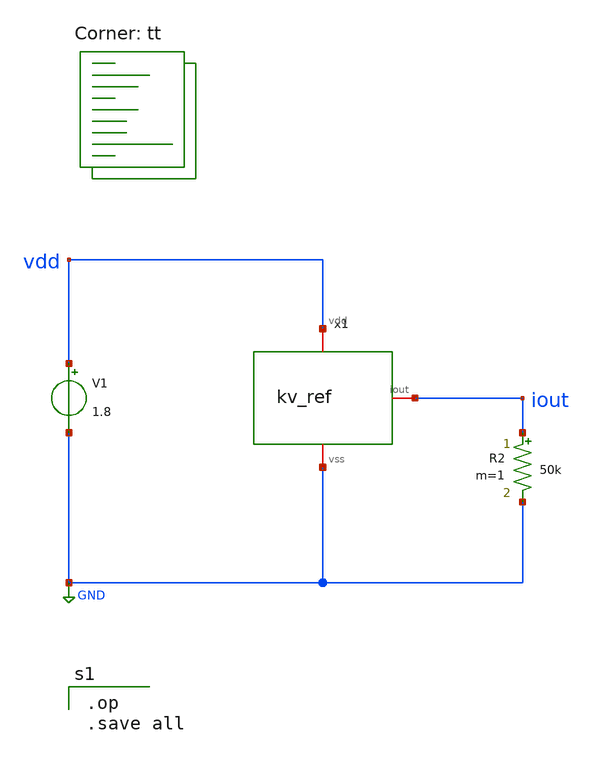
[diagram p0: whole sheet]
** sch_path: examples/demo_tapeout/xschem/tb_ref.sch
**.subckt tb_ref
V1 vdd GND 1.8
x1 vdd GND iout kv_ref
R2 iout GND 50k m=1
**** begin user architecture code
.lib $::SKYWATER_MODELS/sky130.lib.spice tt

.op
.save all

**** end user architecture code
**.ends

* expanding   symbol:  kv_ref.sym # of pins=3
** sym_path: examples/demo_tapeout/xschem/kv_ref.sym
** sch_path: examples/demo_tapeout/xschem/kv_ref.sch
.subckt kv_ref vdd vss iout
*.iopin vdd
*.iopin vss
*.iopin iout
XM3 n1 n2 vdd vdd sky130_fd_pr__pfet_01v8 L=2 W=8 nf=1 ad='int((nf+1)/2) * W/nf * 0.29' as='int((nf+2)/2) * W/nf * 0.29'
+ pd='2*int((nf+1)/2) * (W/nf + 0.29)' ps='2*int((nf+2)/2) * (W/nf + 0.29)' nrd='0.29 / W' nrs='0.29 / W'
+ sa=0 sb=0 sd=0 mult=1 m=1
XM4 n2 n2 vdd vdd sky130_fd_pr__pfet_01v8 L=2 W=8 nf=1 ad='int((nf+1)/2) * W/nf * 0.29' as='int((nf+2)/2) * W/nf * 0.29'
+ pd='2*int((nf+1)/2) * (W/nf + 0.29)' ps='2*int((nf+2)/2) * (W/nf + 0.29)' nrd='0.29 / W' nrs='0.29 / W'
+ sa=0 sb=0 sd=0 mult=1 m=1
XM5 iout n2 vdd vdd sky130_fd_pr__pfet_01v8 L=2 W=8 nf=1 ad='int((nf+1)/2) * W/nf * 0.29' as='int((nf+2)/2) * W/nf * 0.29'
+ pd='2*int((nf+1)/2) * (W/nf + 0.29)' ps='2*int((nf+2)/2) * (W/nf + 0.29)' nrd='0.29 / W' nrs='0.29 / W'
+ sa=0 sb=0 sd=0 mult=1 m=1
XM1 n1 n1 vss vss sky130_fd_pr__nfet_01v8 L=2 W=4 nf=1 ad='int((1 + 1)/2) * 4 / 1 * 0.29' as='int((1 + 2)/2) * 4 / 1 * 0.29'
+ pd='2*int((1 + 1)/2) * (4 / 1 + 0.29)' ps='2*int((1 + 2)/2) * (4 / 1 + 0.29)' nrd='0.29 / 4 ' nrs='0.29 / 4 '
+ sa=0 sb=0 sd=0 mult=1 m=1
XM2 n2 n1 s2 vss sky130_fd_pr__nfet_01v8 L=2 W=16 nf=1 ad='int((1 + 1)/2) * 16 / 1 * 0.29' as='int((1 + 2)/2) * 16 / 1 * 0.29'
+ pd='2*int((1 + 1)/2) * (16 / 1 + 0.29)' ps='2*int((1 + 2)/2) * (16 / 1 + 0.29)' nrd='0.29 / 16 ' nrs='0.29 / 16 '
+ sa=0 sb=0 sd=0 mult=1 m=1
R1 s2 vss 20k m=1
.ends

.GLOBAL GND
.end
